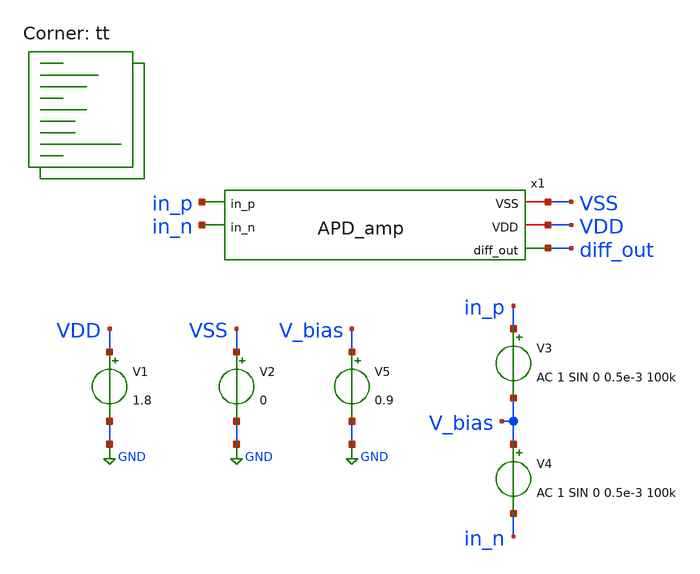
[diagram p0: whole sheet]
** sch_path: xschem/amp_test.sch
**.subckt amp_test
V1 VDD GND 1.8
V2 VSS GND 0
V4 V_bias in_n AC 1 SIN 0 0.5e-3 100k
V3 in_p V_bias AC 1 SIN 0 0.5e-3 100k
V5 V_bias GND 0.9
x1 in_p in_n VSS VDD diff_out APD_amp
**** begin user architecture code
.lib $::SKYWATER_MODELS/sky130.lib.spice tt



* ngspice commands
.options method=gear

.control
save all
tran 0.1u 100u 0
plot v(diff_out) v(in_p) v(in_n)

ac dec 20 1 1e12
plot db(diff_out) db(in_p) db(in_n)

* write amp_test.raw
.endc



**** end user architecture code
**.ends

* expanding   symbol:  APD_amp.sym # of pins=5
** sym_path: xschem/APD_amp.sym
** sch_path: xschem/APD_amp.sch
.subckt APD_amp in_p in_n VSS VDD diff_out
*.iopin VDD
*.ipin in_n
*.ipin in_p
*.opin diff_out
*.iopin VSS
XM3 net2 VDD VSS VSS sky130_fd_pr__nfet_01v8_lvt L=0.15 W=1 nf=1 ad='int((nf+1)/2) * W/nf * 0.29' as='int((nf+2)/2) * W/nf * 0.29'
+ pd='2*int((nf+1)/2) * (W/nf + 0.29)' ps='2*int((nf+2)/2) * (W/nf + 0.29)' nrd='0.29 / W' nrs='0.29 / W'
+ sa=0 sb=0 sd=0 mult=1 m=1
XM1 VDD VDD VSS VSS sky130_fd_pr__nfet_01v8_lvt L=0.15 W=1 nf=1 ad='int((nf+1)/2) * W/nf * 0.29' as='int((nf+2)/2) * W/nf * 0.29'
+ pd='2*int((nf+1)/2) * (W/nf + 0.29)' ps='2*int((nf+2)/2) * (W/nf + 0.29)' nrd='0.29 / W' nrs='0.29 / W'
+ sa=0 sb=0 sd=0 mult=1 m=1
XM2 VDD net1 net1 net4 sky130_fd_pr__pfet_01v8 L=0.15 W=1 nf=1 ad='int((nf+1)/2) * W/nf * 0.29' as='int((nf+2)/2) * W/nf * 0.29'
+ pd='2*int((nf+1)/2) * (W/nf + 0.29)' ps='2*int((nf+2)/2) * (W/nf + 0.29)' nrd='0.29 / W' nrs='0.29 / W'
+ sa=0 sb=0 sd=0 mult=1 m=1
XM5 VDD net1 net3 net5 sky130_fd_pr__pfet_01v8 L=0.15 W=1 nf=1 ad='int((nf+1)/2) * W/nf * 0.29' as='int((nf+2)/2) * W/nf * 0.29'
+ pd='2*int((nf+1)/2) * (W/nf + 0.29)' ps='2*int((nf+2)/2) * (W/nf + 0.29)' nrd='0.29 / W' nrs='0.29 / W'
+ sa=0 sb=0 sd=0 mult=1 m=1
XM6 net3 in_n net2 VSS sky130_fd_pr__nfet_01v8_lvt L=0.15 W=3 nf=1 ad='int((nf+1)/2) * W/nf * 0.29' as='int((nf+2)/2) * W/nf * 0.29'
+ pd='2*int((nf+1)/2) * (W/nf + 0.29)' ps='2*int((nf+2)/2) * (W/nf + 0.29)' nrd='0.29 / W' nrs='0.29 / W'
+ sa=0 sb=0 sd=0 mult=1 m=1
XM4 net1 in_p net2 VSS sky130_fd_pr__nfet_01v8_lvt L=0.15 W=3 nf=1 ad='int((nf+1)/2) * W/nf * 0.29' as='int((nf+2)/2) * W/nf * 0.29'
+ pd='2*int((nf+1)/2) * (W/nf + 0.29)' ps='2*int((nf+2)/2) * (W/nf + 0.29)' nrd='0.29 / W' nrs='0.29 / W'
+ sa=0 sb=0 sd=0 mult=1 m=1
XM7 diff_out net3 VDD VDD sky130_fd_pr__pfet_01v8 L=0.15 W=8 nf=1 ad='int((nf+1)/2) * W/nf * 0.29' as='int((nf+2)/2) * W/nf * 0.29'
+ pd='2*int((nf+1)/2) * (W/nf + 0.29)' ps='2*int((nf+2)/2) * (W/nf + 0.29)' nrd='0.29 / W' nrs='0.29 / W'
+ sa=0 sb=0 sd=0 mult=1 m=1
XM8 diff_out VDD VSS VSS sky130_fd_pr__nfet_01v8_lvt L=0.15 W=0.98 nf=1 ad='int((nf+1)/2) * W/nf * 0.29'
+ as='int((nf+2)/2) * W/nf * 0.29' pd='2*int((nf+1)/2) * (W/nf + 0.29)' ps='2*int((nf+2)/2) * (W/nf + 0.29)'
+ nrd='0.29 / W' nrs='0.29 / W' sa=0 sb=0 sd=0 mult=1 m=1
.ends

.GLOBAL GND
.end
